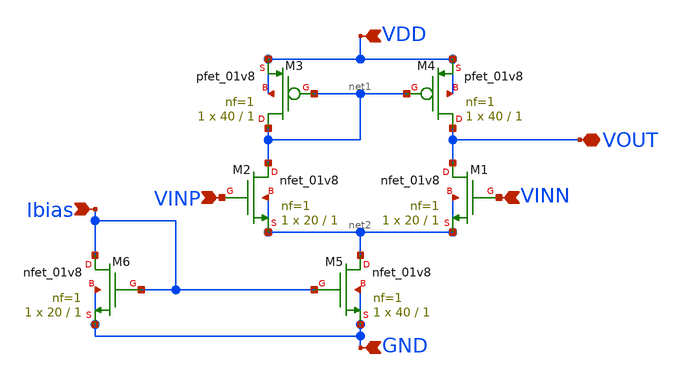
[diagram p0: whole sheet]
** sch_path: high_speed/5tota_high_speed.sch
**.subckt 5tota_high_speed VDD GND VINP VINN VOUT Ibias
*.ipin VDD
*.ipin GND
*.ipin VINP
*.ipin VINN
*.iopin VOUT
*.ipin Ibias
XM2 net1 VINP net2 net2 sky130_fd_pr__nfet_01v8 L=1 W=20 nf=1 ad='int((1 + 1)/2) * 20 / 1 * 0.29' as='int((1 + 2)/2) * 20 / 1 * 0.29'
+ pd='2*int((1 + 1)/2) * (20 / 1 + 0.29)' ps='2*int((1 + 2)/2) * (20 / 1 + 0.29)' nrd='0.29 / 20 ' nrs='0.29 / 20 '
+ sa=0 sb=0 sd=0 mult=1 m=1
XM1 VOUT VINN net2 net2 sky130_fd_pr__nfet_01v8 L=1 W=20 nf=1 ad='int((1 + 1)/2) * 20 / 1 * 0.29' as='int((1 + 2)/2) * 20 / 1 * 0.29'
+ pd='2*int((1 + 1)/2) * (20 / 1 + 0.29)' ps='2*int((1 + 2)/2) * (20 / 1 + 0.29)' nrd='0.29 / 20 ' nrs='0.29 / 20 '
+ sa=0 sb=0 sd=0 mult=1 m=1
XM5 net2 Ibias GND GND sky130_fd_pr__nfet_01v8 L=1 W=40 nf=1 ad='int((1 + 1)/2) * 40 / 1 * 0.29' as='int((1 + 2)/2) * 40 / 1 * 0.29'
+ pd='2*int((1 + 1)/2) * (40 / 1 + 0.29)' ps='2*int((1 + 2)/2) * (40 / 1 + 0.29)' nrd='0.29 / 40 ' nrs='0.29 / 40 '
+ sa=0 sb=0 sd=0 mult=1 m=1
XM3 net1 net1 VDD VDD sky130_fd_pr__pfet_01v8 L=1 W=40 nf=1 ad='int((1 + 1)/2) * 40 / 1 * 0.29' as='int((1 + 2)/2) * 40 / 1 * 0.29'
+ pd='2*int((1 + 1)/2) * (40 / 1 + 0.29)' ps='2*int((1 + 2)/2) * (40 / 1 + 0.29)' nrd='0.29 / 40 ' nrs='0.29 / 40 '
+ sa=0 sb=0 sd=0 mult=1 m=1
XM4 VOUT net1 VDD VDD sky130_fd_pr__pfet_01v8 L=1 W=40 nf=1 ad='int((1 + 1)/2) * 40 / 1 * 0.29' as='int((1 + 2)/2) * 40 / 1 * 0.29'
+ pd='2*int((1 + 1)/2) * (40 / 1 + 0.29)' ps='2*int((1 + 2)/2) * (40 / 1 + 0.29)' nrd='0.29 / 40 ' nrs='0.29 / 40 '
+ sa=0 sb=0 sd=0 mult=1 m=1
XM6 Ibias Ibias GND GND sky130_fd_pr__nfet_01v8 L=1 W=20 nf=1 ad='int((1 + 1)/2) * 20 / 1 * 0.29' as='int((1 + 2)/2) * 20 / 1 * 0.29'
+ pd='2*int((1 + 1)/2) * (20 / 1 + 0.29)' ps='2*int((1 + 2)/2) * (20 / 1 + 0.29)' nrd='0.29 / 20 ' nrs='0.29 / 20 '
+ sa=0 sb=0 sd=0 mult=1 m=1
**.ends
.end
